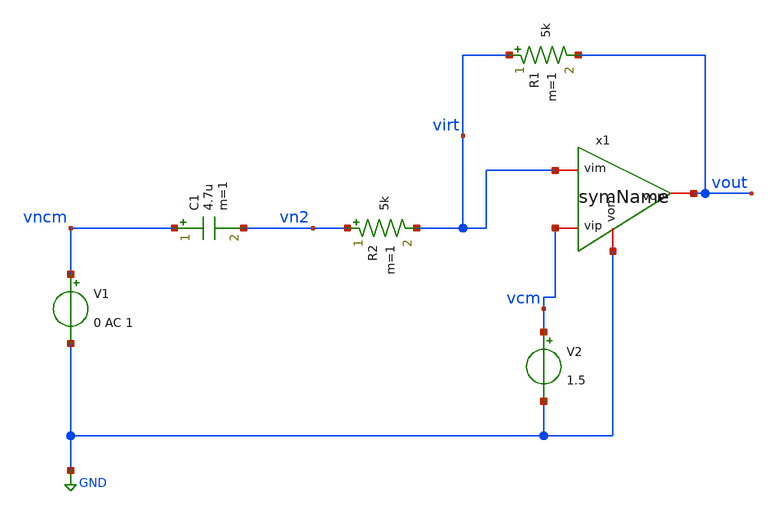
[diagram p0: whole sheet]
** sch_path: xschem/untitled-1.sch
**.subckt untitled-1
V1 vncm GND 0 AC 1
C1 vncm vn2 4.7u m=1
R2 vn2 virt 5k m=1
R1 virt vout 5k m=1
V2 vcm GND 1.5
x1 vout vcm virt GND symName
**.ends

* expanding   symbol:  symName.sym # of pins=4
** sym_path: xschem/symName.sym
** sch_path: xschem/symName.sch
.subckt symName vop vip vim vom
*.iopin vop
*.iopin vom
*.iopin vip
*.iopin vim
E1 vop vom vip vim 1000
.ends

.GLOBAL GND
.end
